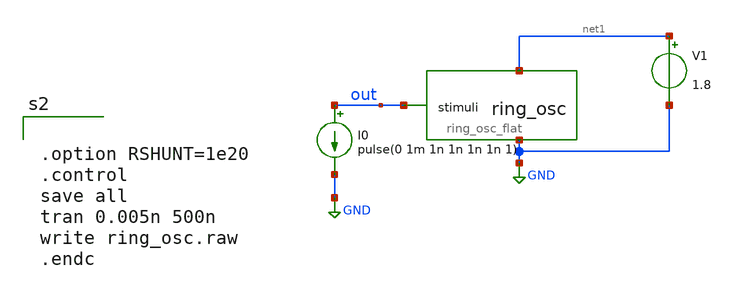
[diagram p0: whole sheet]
** sch_path: xschem/src/ring_osc/ring_osc_tb.sch
**.subckt ring_osc_tb
V1 net1 GND 1.8
I0 out GND pulse(0 1m 1n 1n 1n 1n 1)
x1 net1 out GND ring_osc_flat
**** begin user architecture code


.include /home/eda/magic/ring_osc/ring_osc_flat.spice




.include $::SKYWATER_MODELS/cells/nfet_01v8/sky130_fd_pr__nfet_01v8__tt.corner.spice
.include $::SKYWATER_MODELS/cells/nfet_01v8_lvt/sky130_fd_pr__nfet_01v8_lvt__tt.corner.spice
.include $::SKYWATER_MODELS/cells/pfet_01v8/sky130_fd_pr__pfet_01v8__tt.corner.spice
.include $::SKYWATER_MODELS/cells/nfet_03v3_nvt/sky130_fd_pr__nfet_03v3_nvt__tt.corner.spice
.include $::SKYWATER_MODELS/cells/nfet_05v0_nvt/sky130_fd_pr__nfet_05v0_nvt__tt.corner.spice
.include $::SKYWATER_MODELS/cells/esd_nfet_01v8/sky130_fd_pr__esd_nfet_01v8__tt.corner.spice
.include $::SKYWATER_MODELS/cells/pfet_01v8_lvt/sky130_fd_pr__pfet_01v8_lvt__tt.corner.spice
.include $::SKYWATER_MODELS/cells/pfet_01v8_hvt/sky130_fd_pr__pfet_01v8_hvt__tt.corner.spice
.include $::SKYWATER_MODELS/cells/esd_pfet_g5v0d10v5/sky130_fd_pr__esd_pfet_g5v0d10v5__tt.corner.spice
.include $::SKYWATER_MODELS/cells/pfet_g5v0d10v5/sky130_fd_pr__pfet_g5v0d10v5__tt.corner.spice
.include $::SKYWATER_MODELS/cells/pfet_g5v0d16v0/sky130_fd_pr__pfet_g5v0d16v0__tt.corner.spice
.include $::SKYWATER_MODELS/cells/nfet_g5v0d10v5/sky130_fd_pr__nfet_g5v0d10v5__tt.corner.spice
.include $::SKYWATER_MODELS/cells/nfet_g5v0d16v0/sky130_fd_pr__nfet_g5v0d16v0__tt_discrete.corner.spice
.include $::SKYWATER_MODELS/cells/esd_nfet_g5v0d10v5/sky130_fd_pr__esd_nfet_g5v0d10v5__tt.corner.spice
.include $::SKYWATER_MODELS/models/corners/tt/nonfet.spice
* Mismatch parameters
.include $::SKYWATER_MODELS/cells/nfet_01v8/sky130_fd_pr__nfet_01v8__mismatch.corner.spice
.include $::SKYWATER_MODELS/cells/pfet_01v8/sky130_fd_pr__pfet_01v8__mismatch.corner.spice
.include $::SKYWATER_MODELS/cells/nfet_01v8_lvt/sky130_fd_pr__nfet_01v8_lvt__mismatch.corner.spice
.include $::SKYWATER_MODELS/cells/pfet_01v8_lvt/sky130_fd_pr__pfet_01v8_lvt__mismatch.corner.spice
.include $::SKYWATER_MODELS/cells/pfet_01v8_hvt/sky130_fd_pr__pfet_01v8_hvt__mismatch.corner.spice
.include $::SKYWATER_MODELS/cells/nfet_g5v0d10v5/sky130_fd_pr__nfet_g5v0d10v5__mismatch.corner.spice
.include $::SKYWATER_MODELS/cells/pfet_g5v0d10v5/sky130_fd_pr__pfet_g5v0d10v5__mismatch.corner.spice
.include $::SKYWATER_MODELS/cells/nfet_05v0_nvt/sky130_fd_pr__nfet_05v0_nvt__mismatch.corner.spice
.include $::SKYWATER_MODELS/cells/nfet_03v3_nvt/sky130_fd_pr__nfet_03v3_nvt__mismatch.corner.spice
* Resistor$::SKYWATER_MODELS/Capacitor
.include $::SKYWATER_MODELS/models/r+c/res_typical__cap_typical.spice
.include $::SKYWATER_MODELS/models/r+c/res_typical__cap_typical__lin.spice
* Special cells
.include $::SKYWATER_MODELS/models/corners/tt/specialized_cells.spice
* All models
.include $::SKYWATER_MODELS/models/all.spice
* Corner
.include $::SKYWATER_MODELS/models/corners/tt/rf.spice



.option RSHUNT=1e20
.control
save all
tran 0.005n 500n
write ring_osc.raw
.endc


**** end user architecture code
**.ends
.GLOBAL GND
.end
